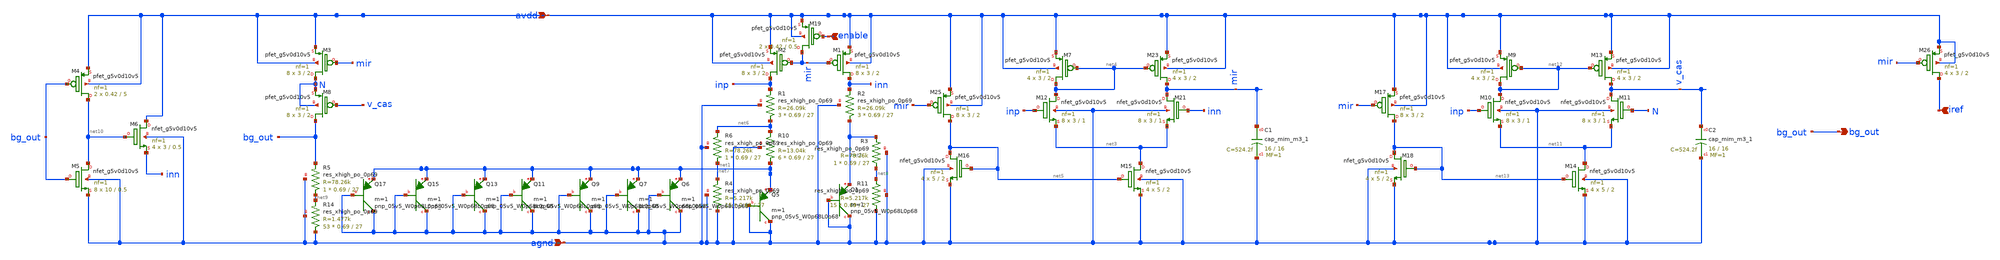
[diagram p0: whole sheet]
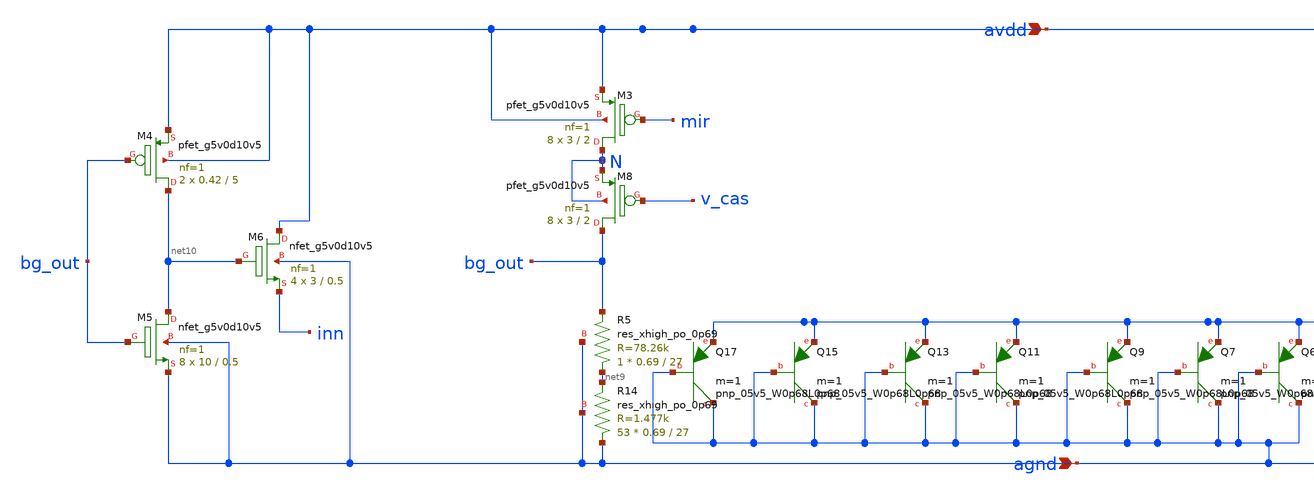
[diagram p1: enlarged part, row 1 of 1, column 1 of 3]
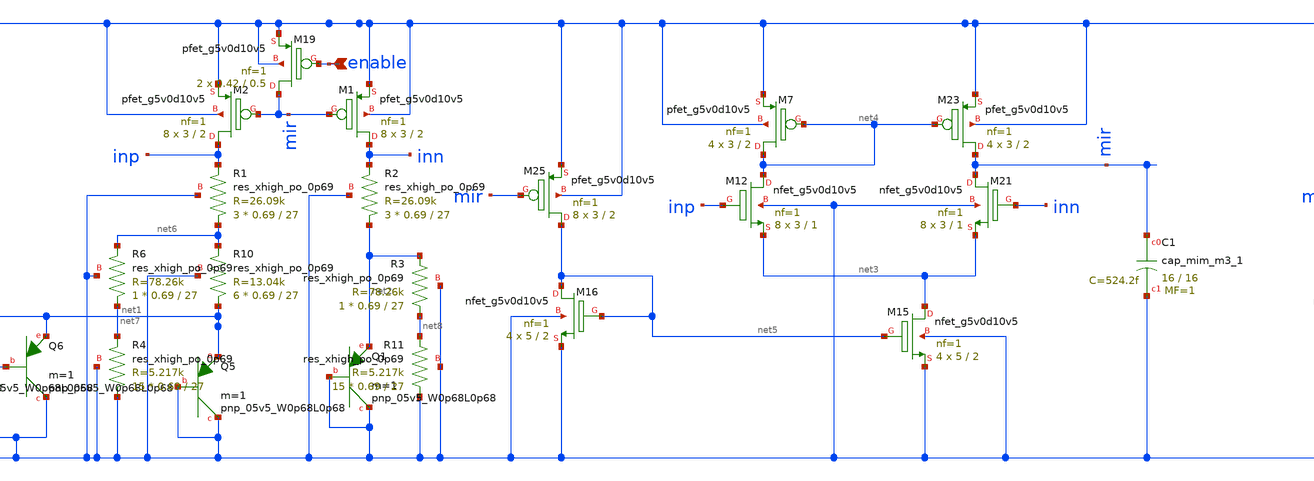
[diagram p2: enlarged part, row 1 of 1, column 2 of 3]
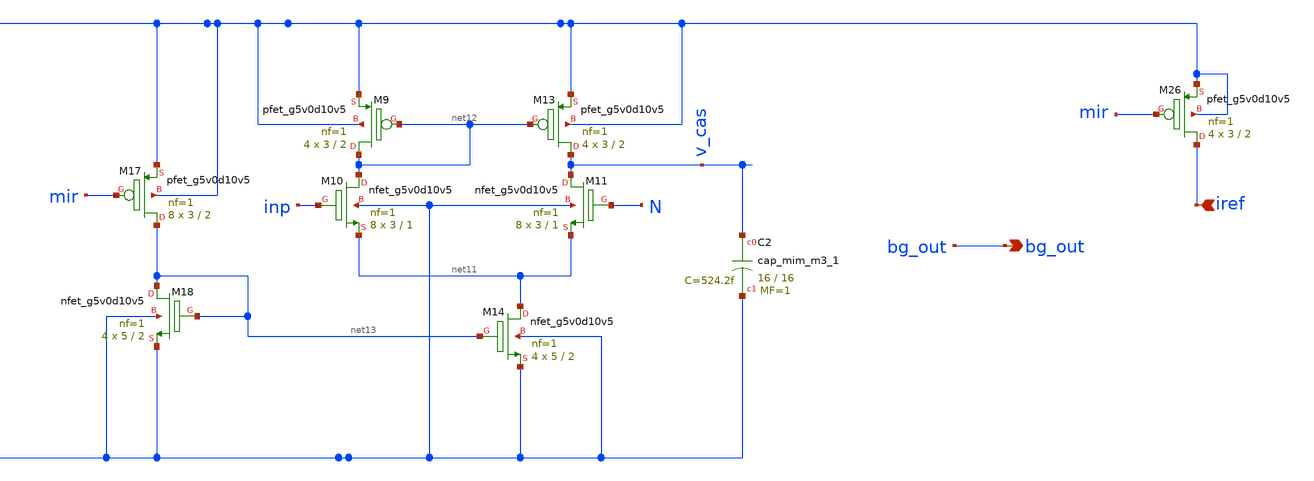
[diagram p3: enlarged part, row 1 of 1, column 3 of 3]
** sch_path: bgr_cascode.sch
**.subckt bgr_cascode avdd agnd bg_out enable iref
*.ipin avdd
*.ipin agnd
*.opin bg_out
*.ipin enable
*.ipin iref
XM1 inn mir avdd avdd sky130_fd_pr__pfet_g5v0d10v5 L=2 W=3 nf=1 ad='int((nf+1)/2) * W/nf * 0.29' as='int((nf+2)/2) * W/nf * 0.29'
+ pd='2*int((nf+1)/2) * (W/nf + 0.29)' ps='2*int((nf+2)/2) * (W/nf + 0.29)' nrd='0.29 / W' nrs='0.29 / W'
+ sa=0 sb=0 sd=0 mult=8 m=8
XM2 inp mir avdd avdd sky130_fd_pr__pfet_g5v0d10v5 L=2 W=3 nf=1 ad='int((nf+1)/2) * W/nf * 0.29' as='int((nf+2)/2) * W/nf * 0.29'
+ pd='2*int((nf+1)/2) * (W/nf + 0.29)' ps='2*int((nf+2)/2) * (W/nf + 0.29)' nrd='0.29 / W' nrs='0.29 / W'
+ sa=0 sb=0 sd=0 mult=8 m=8
XM3 N mir avdd avdd sky130_fd_pr__pfet_g5v0d10v5 L=2 W=3 nf=1 ad='int((nf+1)/2) * W/nf * 0.29' as='int((nf+2)/2) * W/nf * 0.29'
+ pd='2*int((nf+1)/2) * (W/nf + 0.29)' ps='2*int((nf+2)/2) * (W/nf + 0.29)' nrd='0.29 / W' nrs='0.29 / W'
+ sa=0 sb=0 sd=0 mult=8 m=8
XQ1 agnd agnd net2 sky130_fd_pr__pnp_05v5_W0p68L0p68 m=1
XQ5 agnd agnd net1 sky130_fd_pr__pnp_05v5_W0p68L0p68 m=1
XQ6 agnd agnd net1 sky130_fd_pr__pnp_05v5_W0p68L0p68 m=1
XQ7 agnd agnd net1 sky130_fd_pr__pnp_05v5_W0p68L0p68 m=1
XQ9 agnd agnd net1 sky130_fd_pr__pnp_05v5_W0p68L0p68 m=1
XQ11 agnd agnd net1 sky130_fd_pr__pnp_05v5_W0p68L0p68 m=1
XQ13 agnd agnd net1 sky130_fd_pr__pnp_05v5_W0p68L0p68 m=1
XQ15 agnd agnd net1 sky130_fd_pr__pnp_05v5_W0p68L0p68 m=1
XQ17 agnd agnd net1 sky130_fd_pr__pnp_05v5_W0p68L0p68 m=1
XM7 net4 net4 avdd avdd sky130_fd_pr__pfet_g5v0d10v5 L=2 W=3 nf=1 ad='int((nf+1)/2) * W/nf * 0.29' as='int((nf+2)/2) * W/nf * 0.29'
+ pd='2*int((nf+1)/2) * (W/nf + 0.29)' ps='2*int((nf+2)/2) * (W/nf + 0.29)' nrd='0.29 / W' nrs='0.29 / W'
+ sa=0 sb=0 sd=0 mult=4 m=4
XM12 net4 inp net3 agnd sky130_fd_pr__nfet_g5v0d10v5 L=1 W=3 nf=1 ad='int((nf+1)/2) * W/nf * 0.29' as='int((nf+2)/2) * W/nf * 0.29'
+ pd='2*int((nf+1)/2) * (W/nf + 0.29)' ps='2*int((nf+2)/2) * (W/nf + 0.29)' nrd='0.29 / W' nrs='0.29 / W'
+ sa=0 sb=0 sd=0 mult=8 m=8
XM21 mir inn net3 agnd sky130_fd_pr__nfet_g5v0d10v5 L=1 W=3 nf=1 ad='int((nf+1)/2) * W/nf * 0.29' as='int((nf+2)/2) * W/nf * 0.29'
+ pd='2*int((nf+1)/2) * (W/nf + 0.29)' ps='2*int((nf+2)/2) * (W/nf + 0.29)' nrd='0.29 / W' nrs='0.29 / W'
+ sa=0 sb=0 sd=0 mult=8 m=8
XM23 mir net4 avdd avdd sky130_fd_pr__pfet_g5v0d10v5 L=2 W=3 nf=1 ad='int((nf+1)/2) * W/nf * 0.29' as='int((nf+2)/2) * W/nf * 0.29'
+ pd='2*int((nf+1)/2) * (W/nf + 0.29)' ps='2*int((nf+2)/2) * (W/nf + 0.29)' nrd='0.29 / W' nrs='0.29 / W'
+ sa=0 sb=0 sd=0 mult=4 m=4
XM15 net3 net5 agnd agnd sky130_fd_pr__nfet_g5v0d10v5 L=2 W=5 nf=1 ad='int((nf+1)/2) * W/nf * 0.29' as='int((nf+2)/2) * W/nf * 0.29'
+ pd='2*int((nf+1)/2) * (W/nf + 0.29)' ps='2*int((nf+2)/2) * (W/nf + 0.29)' nrd='0.29 / W' nrs='0.29 / W'
+ sa=0 sb=0 sd=0 mult=4 m=4
XM25 net5 mir avdd avdd sky130_fd_pr__pfet_g5v0d10v5 L=2 W=3 nf=1 ad='int((nf+1)/2) * W/nf * 0.29' as='int((nf+2)/2) * W/nf * 0.29'
+ pd='2*int((nf+1)/2) * (W/nf + 0.29)' ps='2*int((nf+2)/2) * (W/nf + 0.29)' nrd='0.29 / W' nrs='0.29 / W'
+ sa=0 sb=0 sd=0 mult=8 m=8
XM16 net5 net5 agnd agnd sky130_fd_pr__nfet_g5v0d10v5 L=2 W=5 nf=1 ad='int((nf+1)/2) * W/nf * 0.29' as='int((nf+2)/2) * W/nf * 0.29'
+ pd='2*int((nf+1)/2) * (W/nf + 0.29)' ps='2*int((nf+2)/2) * (W/nf + 0.29)' nrd='0.29 / W' nrs='0.29 / W'
+ sa=0 sb=0 sd=0 mult=4 m=4
XC1 mir agnd sky130_fd_pr__cap_mim_m3_1 W=16 L=16 MF=1 m=1
XR1 net6 inp agnd sky130_fd_pr__res_xhigh_po_0p69 L=27 mult=3 m=3
XR2 net2 inn agnd sky130_fd_pr__res_xhigh_po_0p69 L=27 mult=3 m=3
XR3 net8 net2 agnd sky130_fd_pr__res_xhigh_po_0p69 L=27 mult=1 m=1
XR10 net1 net6 agnd sky130_fd_pr__res_xhigh_po_0p69 L=27 mult=6 m=6
XR4 agnd net7 agnd sky130_fd_pr__res_xhigh_po_0p69 L=27 mult=15 m=15
XR11 agnd net8 agnd sky130_fd_pr__res_xhigh_po_0p69 L=27 mult=15 m=15
XR6 net7 net6 agnd sky130_fd_pr__res_xhigh_po_0p69 L=27 mult=1 m=1
XR5 net9 bg_out agnd sky130_fd_pr__res_xhigh_po_0p69 L=27 mult=1 m=1
XR14 agnd net9 agnd sky130_fd_pr__res_xhigh_po_0p69 L=27 mult=53 m=53
XM19 mir enable avdd avdd sky130_fd_pr__pfet_g5v0d10v5 L=0.5 W=0.42 nf=1 ad='int((nf+1)/2) * W/nf * 0.29'
+ as='int((nf+2)/2) * W/nf * 0.29' pd='2*int((nf+1)/2) * (W/nf + 0.29)' ps='2*int((nf+2)/2) * (W/nf + 0.29)'
+ nrd='0.29 / W' nrs='0.29 / W' sa=0 sb=0 sd=0 mult=2 m=2
XM4 net10 bg_out avdd avdd sky130_fd_pr__pfet_g5v0d10v5 L=5 W=0.42 nf=1 ad='int((nf+1)/2) * W/nf * 0.29'
+ as='int((nf+2)/2) * W/nf * 0.29' pd='2*int((nf+1)/2) * (W/nf + 0.29)' ps='2*int((nf+2)/2) * (W/nf + 0.29)'
+ nrd='0.29 / W' nrs='0.29 / W' sa=0 sb=0 sd=0 mult=2 m=2
XM5 net10 bg_out agnd agnd sky130_fd_pr__nfet_g5v0d10v5 L=0.5 W=10 nf=1 ad='int((nf+1)/2) * W/nf * 0.29'
+ as='int((nf+2)/2) * W/nf * 0.29' pd='2*int((nf+1)/2) * (W/nf + 0.29)' ps='2*int((nf+2)/2) * (W/nf + 0.29)'
+ nrd='0.29 / W' nrs='0.29 / W' sa=0 sb=0 sd=0 mult=8 m=8
XM6 avdd net10 inn agnd sky130_fd_pr__nfet_g5v0d10v5 L=0.5 W=3 nf=1 ad='int((nf+1)/2) * W/nf * 0.29'
+ as='int((nf+2)/2) * W/nf * 0.29' pd='2*int((nf+1)/2) * (W/nf + 0.29)' ps='2*int((nf+2)/2) * (W/nf + 0.29)'
+ nrd='0.29 / W' nrs='0.29 / W' sa=0 sb=0 sd=0 mult=4 m=4
XM26 iref mir avdd avdd sky130_fd_pr__pfet_g5v0d10v5 L=2 W=3 nf=1 ad='int((nf+1)/2) * W/nf * 0.29' as='int((nf+2)/2) * W/nf * 0.29'
+ pd='2*int((nf+1)/2) * (W/nf + 0.29)' ps='2*int((nf+2)/2) * (W/nf + 0.29)' nrd='0.29 / W' nrs='0.29 / W'
+ sa=0 sb=0 sd=0 mult=4 m=4
XM9 net12 net12 avdd avdd sky130_fd_pr__pfet_g5v0d10v5 L=2 W=3 nf=1 ad='int((nf+1)/2) * W/nf * 0.29'
+ as='int((nf+2)/2) * W/nf * 0.29' pd='2*int((nf+1)/2) * (W/nf + 0.29)' ps='2*int((nf+2)/2) * (W/nf + 0.29)'
+ nrd='0.29 / W' nrs='0.29 / W' sa=0 sb=0 sd=0 mult=4 m=4
XM10 net12 inp net11 agnd sky130_fd_pr__nfet_g5v0d10v5 L=1 W=3 nf=1 ad='int((nf+1)/2) * W/nf * 0.29'
+ as='int((nf+2)/2) * W/nf * 0.29' pd='2*int((nf+1)/2) * (W/nf + 0.29)' ps='2*int((nf+2)/2) * (W/nf + 0.29)'
+ nrd='0.29 / W' nrs='0.29 / W' sa=0 sb=0 sd=0 mult=8 m=8
XM11 v_cas N net11 agnd sky130_fd_pr__nfet_g5v0d10v5 L=1 W=3 nf=1 ad='int((nf+1)/2) * W/nf * 0.29' as='int((nf+2)/2) * W/nf * 0.29'
+ pd='2*int((nf+1)/2) * (W/nf + 0.29)' ps='2*int((nf+2)/2) * (W/nf + 0.29)' nrd='0.29 / W' nrs='0.29 / W'
+ sa=0 sb=0 sd=0 mult=8 m=8
XM13 v_cas net12 avdd avdd sky130_fd_pr__pfet_g5v0d10v5 L=2 W=3 nf=1 ad='int((nf+1)/2) * W/nf * 0.29'
+ as='int((nf+2)/2) * W/nf * 0.29' pd='2*int((nf+1)/2) * (W/nf + 0.29)' ps='2*int((nf+2)/2) * (W/nf + 0.29)'
+ nrd='0.29 / W' nrs='0.29 / W' sa=0 sb=0 sd=0 mult=4 m=4
XM14 net11 net13 agnd agnd sky130_fd_pr__nfet_g5v0d10v5 L=2 W=5 nf=1 ad='int((nf+1)/2) * W/nf * 0.29'
+ as='int((nf+2)/2) * W/nf * 0.29' pd='2*int((nf+1)/2) * (W/nf + 0.29)' ps='2*int((nf+2)/2) * (W/nf + 0.29)'
+ nrd='0.29 / W' nrs='0.29 / W' sa=0 sb=0 sd=0 mult=4 m=4
XM17 net13 mir avdd avdd sky130_fd_pr__pfet_g5v0d10v5 L=2 W=3 nf=1 ad='int((nf+1)/2) * W/nf * 0.29' as='int((nf+2)/2) * W/nf * 0.29'
+ pd='2*int((nf+1)/2) * (W/nf + 0.29)' ps='2*int((nf+2)/2) * (W/nf + 0.29)' nrd='0.29 / W' nrs='0.29 / W'
+ sa=0 sb=0 sd=0 mult=8 m=8
XM18 net13 net13 agnd agnd sky130_fd_pr__nfet_g5v0d10v5 L=2 W=5 nf=1 ad='int((nf+1)/2) * W/nf * 0.29'
+ as='int((nf+2)/2) * W/nf * 0.29' pd='2*int((nf+1)/2) * (W/nf + 0.29)' ps='2*int((nf+2)/2) * (W/nf + 0.29)'
+ nrd='0.29 / W' nrs='0.29 / W' sa=0 sb=0 sd=0 mult=4 m=4
XC2 v_cas agnd sky130_fd_pr__cap_mim_m3_1 W=16 L=16 MF=1 m=1
XM8 bg_out v_cas N N sky130_fd_pr__pfet_g5v0d10v5 L=2 W=3 nf=1 ad='int((nf+1)/2) * W/nf * 0.29' as='int((nf+2)/2) * W/nf * 0.29'
+ pd='2*int((nf+1)/2) * (W/nf + 0.29)' ps='2*int((nf+2)/2) * (W/nf + 0.29)' nrd='0.29 / W' nrs='0.29 / W'
+ sa=0 sb=0 sd=0 mult=8 m=8
**.ends
.end
